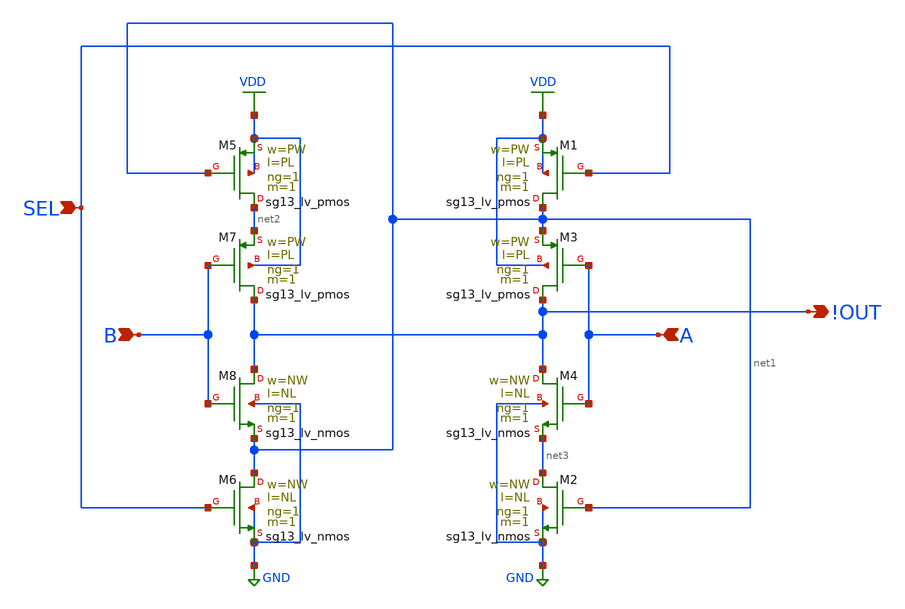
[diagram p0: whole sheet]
** sch_path: Tile/include/cmos5l/konrads_cells/sch/mux_inv.sch
**.subckt mux_inv B A SEL !OUT
*.ipin B
*.ipin A
*.ipin SEL
*.opin !OUT
XM5 net2 net1 VDD VDD sg13_lv_pmos w=PW l=PL ng=1 m=1 mm_ok=1
XM6 net1 SEL GND GND sg13_lv_nmos w=NW l=NL ng=1 m=1 mm_ok=1
XM7 !OUT B net2 VDD sg13_lv_pmos w=PW l=PL ng=1 m=1 mm_ok=1
XM8 !OUT B net1 GND sg13_lv_nmos w=NW l=NL ng=1 m=1 mm_ok=1
XM1 net1 SEL VDD VDD sg13_lv_pmos w=PW l=PL ng=1 m=1 mm_ok=1
XM2 net3 net1 GND GND sg13_lv_nmos w=NW l=NL ng=1 m=1 mm_ok=1
XM3 !OUT A net1 VDD sg13_lv_pmos w=PW l=PL ng=1 m=1 mm_ok=1
XM4 !OUT A net3 GND sg13_lv_nmos w=NW l=NL ng=1 m=1 mm_ok=1
**.ends
.GLOBAL VDD
.GLOBAL GND
.end
